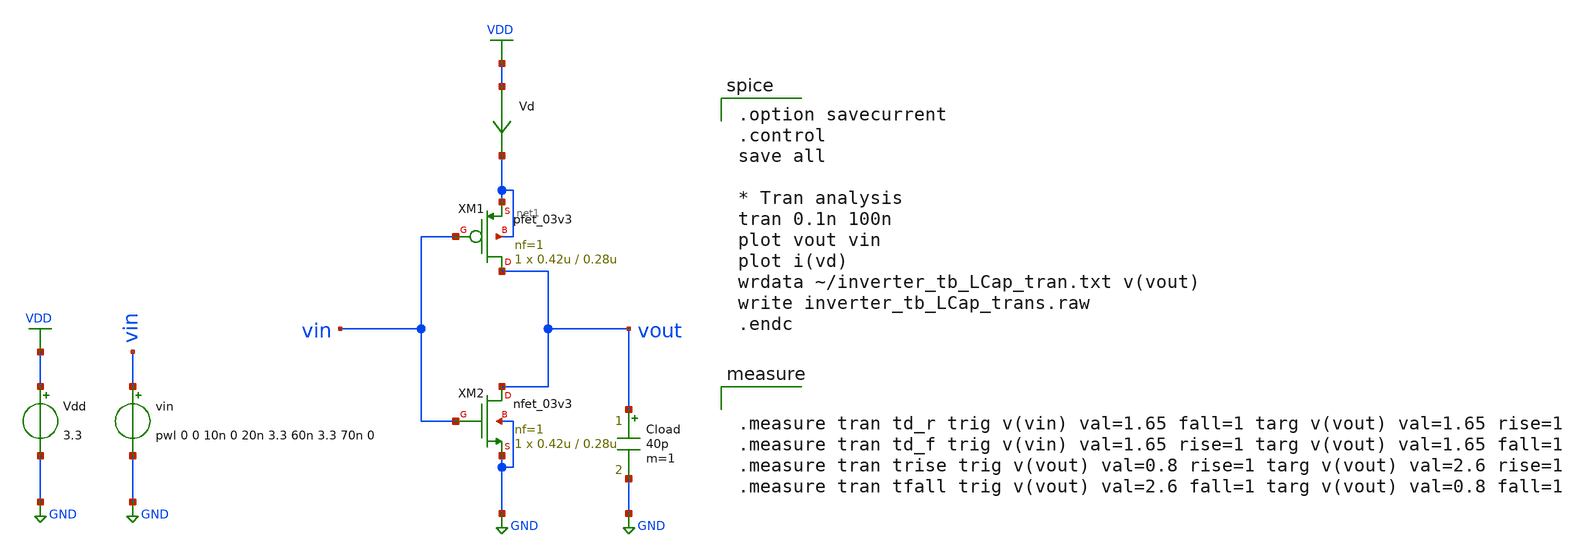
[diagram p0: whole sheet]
** sch_path: samples/inverter/GF180/inverter_tb_LCap_trans.sch
**.subckt inverter_tb_LCap_trans
Vdd VDD GND 3.3
vin vin GND pwl 0 0 10n 0 20n 3.3 60n 3.3 70n 0
Vd VDD net1 0
.save i(vd)
Cload vout GND 40p m=1
XM1 vout vin net1 net1 pfet_03v3 L=0.28u W=0.42u nf=1 ad='int((nf+1)/2) * W/nf * 0.18u' as='int((nf+2)/2) * W/nf * 0.18u'
+ pd='2*int((nf+1)/2) * (W/nf + 0.18u)' ps='2*int((nf+2)/2) * (W/nf + 0.18u)' nrd='0.18u / W' nrs='0.18u / W'
+ sa=0 sb=0 sd=0 m=1
XM2 vout vin GND GND nfet_03v3 L=0.28u W=0.42u nf=1 ad='int((nf+1)/2) * W/nf * 0.18u' as='int((nf+2)/2) * W/nf * 0.18u'
+ pd='2*int((nf+1)/2) * (W/nf + 0.18u)' ps='2*int((nf+2)/2) * (W/nf + 0.18u)' nrd='0.18u / W' nrs='0.18u / W'
+ sa=0 sb=0 sd=0 m=1
**** begin user architecture code

.option savecurrent
.control
save all

* Tran analysis
tran 0.1n 100n
plot vout vin
plot i(vd)
wrdata ~/inverter_tb_LCap_tran.txt v(vout)
write inverter_tb_LCap_trans.raw
.endc



.measure tran td_r trig v(vin) val=1.65 fall=1 targ v(vout) val=1.65 rise=1
.measure tran td_f trig v(vin) val=1.65 rise=1 targ v(vout) val=1.65 fall=1
.measure tran trise trig v(vout) val=0.8 rise=1 targ v(vout) val=2.6 rise=1
.measure tran tfall trig v(vout) val=2.6 fall=1 targ v(vout) val=0.8 fall=1



.include $::180MCU_MODELS/design.ngspice
.lib $::180MCU_MODELS/sm141064.ngspice typical
.lib $::180MCU_MODELS/sm141064.ngspice res_typical
.lib $::180MCU_MODELS/sm141064.ngspice moscap_typical
.lib $::180MCU_MODELS/sm141064.ngspice diode_typical
* .lib $::180MCU_MODELS/sm141064.ngspice res_statistical

**** end user architecture code
**.ends
.GLOBAL VDD
.GLOBAL GND
.end
